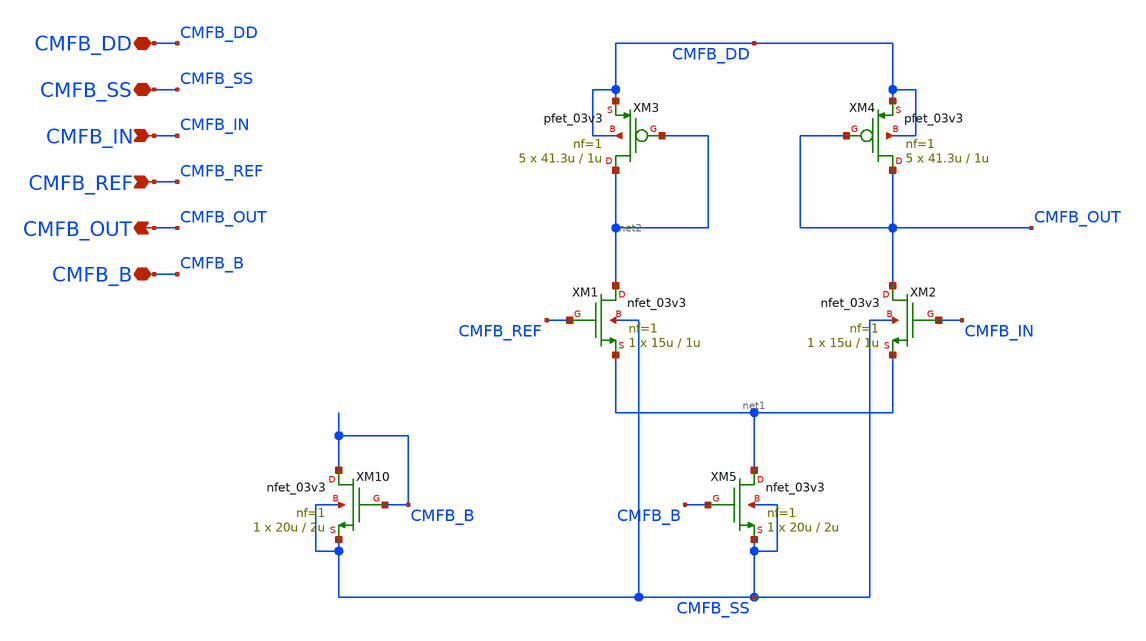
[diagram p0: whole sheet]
** sch_path: Design_Files/IC Design/Schematic/ANALOG_BLOCKS/FD_OTA/CMFB/CMFB.sch
**.subckt CMFB CMFB_DD CMFB_SS CMFB_IN CMFB_REF CMFB_OUT CMFB_B
*.iopin CMFB_DD
*.iopin CMFB_SS
*.ipin CMFB_IN
*.ipin CMFB_REF
*.opin CMFB_OUT
*.iopin CMFB_B
XM4 CMFB_OUT CMFB_OUT CMFB_DD CMFB_DD pfet_03v3 L=1u W=41.3u nf=1 ad='int((nf+1)/2) * W/nf * 0.18u' as='int((nf+2)/2) * W/nf * 0.18u'
+ pd='2*int((nf+1)/2) * (W/nf + 0.18u)' ps='2*int((nf+2)/2) * (W/nf + 0.18u)' nrd='0.18u / W' nrs='0.18u / W'
+ sa=0 sb=0 sd=0 m=5
XM3 net2 net2 CMFB_DD CMFB_DD pfet_03v3 L=1u W=41.3u nf=1 ad='int((nf+1)/2) * W/nf * 0.18u' as='int((nf+2)/2) * W/nf * 0.18u'
+ pd='2*int((nf+1)/2) * (W/nf + 0.18u)' ps='2*int((nf+2)/2) * (W/nf + 0.18u)' nrd='0.18u / W' nrs='0.18u / W'
+ sa=0 sb=0 sd=0 m=5
XM1 net2 CMFB_REF net1 CMFB_SS nfet_03v3 L=1u W=15u nf=1 ad='int((nf+1)/2) * W/nf * 0.18u' as='int((nf+2)/2) * W/nf * 0.18u'
+ pd='2*int((nf+1)/2) * (W/nf + 0.18u)' ps='2*int((nf+2)/2) * (W/nf + 0.18u)' nrd='0.18u / W' nrs='0.18u / W'
+ sa=0 sb=0 sd=0 m=1
XM2 CMFB_OUT CMFB_IN net1 CMFB_SS nfet_03v3 L=1u W=15u nf=1 ad='int((nf+1)/2) * W/nf * 0.18u' as='int((nf+2)/2) * W/nf * 0.18u'
+ pd='2*int((nf+1)/2) * (W/nf + 0.18u)' ps='2*int((nf+2)/2) * (W/nf + 0.18u)' nrd='0.18u / W' nrs='0.18u / W'
+ sa=0 sb=0 sd=0 m=1
XM5 net1 CMFB_B CMFB_SS CMFB_SS nfet_03v3 L=2u W=20u nf=1 ad='int((nf+1)/2) * W/nf * 0.18u' as='int((nf+2)/2) * W/nf * 0.18u'
+ pd='2*int((nf+1)/2) * (W/nf + 0.18u)' ps='2*int((nf+2)/2) * (W/nf + 0.18u)' nrd='0.18u / W' nrs='0.18u / W'
+ sa=0 sb=0 sd=0 m=1
XM10 CMFB_B CMFB_B CMFB_SS CMFB_SS nfet_03v3 L=2u W=20u nf=1 ad='int((nf+1)/2) * W/nf * 0.18u' as='int((nf+2)/2) * W/nf * 0.18u'
+ pd='2*int((nf+1)/2) * (W/nf + 0.18u)' ps='2*int((nf+2)/2) * (W/nf + 0.18u)' nrd='0.18u / W' nrs='0.18u / W'
+ sa=0 sb=0 sd=0 m=1
**.ends
.end
